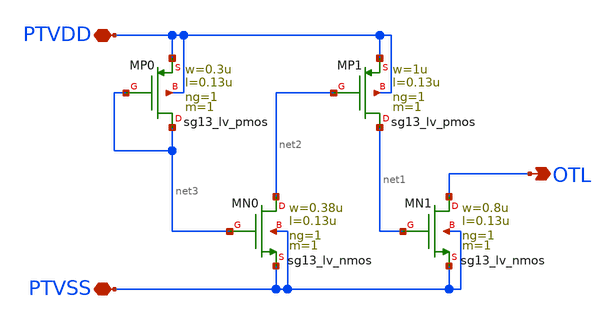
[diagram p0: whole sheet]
** sch_path: xschem/tie_low.sch
**.subckt tie_low PTVDD PTVSS OTL
*.iopin PTVDD
*.iopin PTVSS
*.opin OTL
XMN0 net2 net3 PTVSS PTVSS sg13_lv_nmos w=0.38u l=0.13u ng=1 m=1 mm_ok=1
XMP1 net1 net2 PTVDD PTVDD sg13_lv_pmos w=1u l=0.13u ng=1 m=1 mm_ok=1
XMN1 OTL net1 PTVSS PTVSS sg13_lv_nmos w=0.8u l=0.13u ng=1 m=1 mm_ok=1
XMP0 net3 net3 PTVDD PTVDD sg13_lv_pmos w=0.3u l=0.13u ng=1 m=1 mm_ok=1
**.ends
.end
